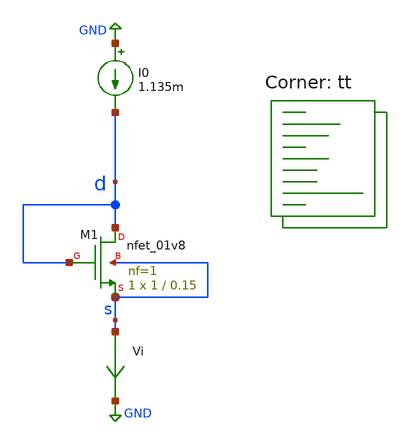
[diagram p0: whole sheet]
** sch_path: opanalysis.sch
**.subckt opanalysis
XM1 d d s s sky130_fd_pr__nfet_01v8 L=0.15 W=1 nf=1 ad='int((nf+1)/2) * W/nf * 0.29' as='int((nf+2)/2) * W/nf * 0.29'
+ pd='2*int((nf+1)/2) * (W/nf + 0.29)' ps='2*int((nf+2)/2) * (W/nf + 0.29)' nrd='0.29 / W' nrs='0.29 / W'
+ sa=0 sb=0 sd=0 mult=1 m=1
I0 GND d 1.135m
Vi s GND 0
.save i(vi)
**** begin user architecture code
.lib $::SKYWATER_MODELS/sky130.lib.spice tt



.option savecurrents

.control

save all

save @m.xm1.msky130_fd_pr__nfet_01v8[gm]
save @m.xm1.msky130_fd_pr__nfet_01v8[vth]
*save @m.xm1.msky130_fd_pr__nfet_01v8[id]

*set appendwrite

op
*write opanalysis.raw

.endc



**** end user architecture code
**.ends
.GLOBAL GND
.end
